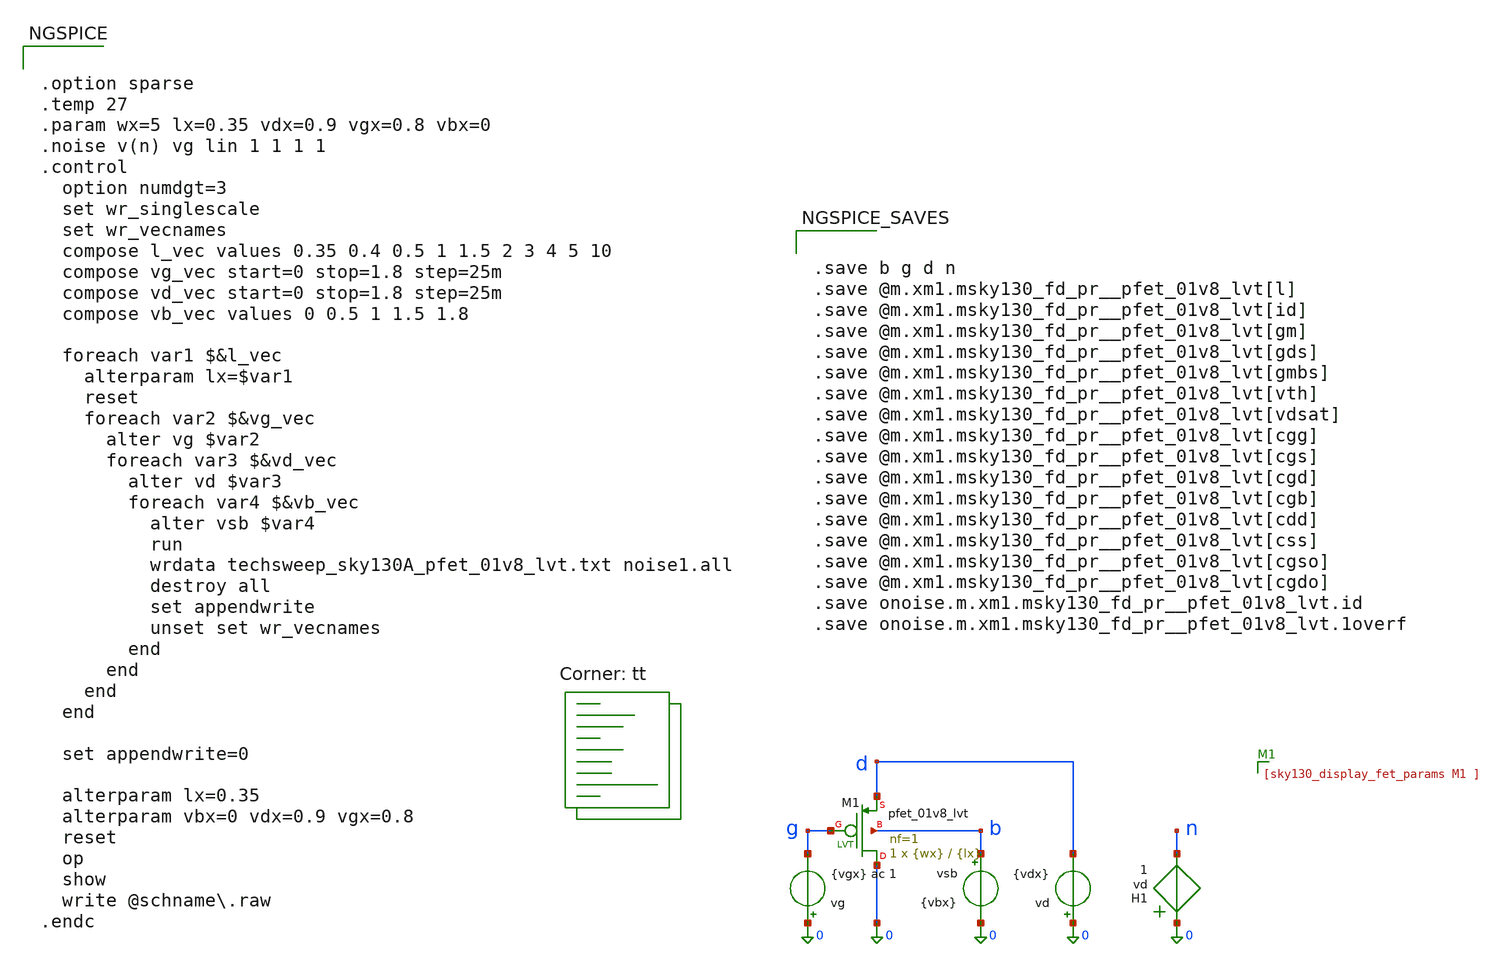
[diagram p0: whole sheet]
** sch_path: sch/gmid/gmid_pmos_lv.sch
**.subckt gmid_pmos_lv
vsb b 0 {vbx}
vd 0 d {vdx}
vg 0 g {vgx} ac 1
H1 0 n vd 1
XM1 0 g d b sky130_fd_pr__pfet_01v8_lvt L={lx} W={wx} nf=1 ad='int((1 + 1)/2) * {wx} / 1 * 0.29' as='int((1 + 2)/2) * {wx} / 1 * 0.29'
+ pd='2*int((1 + 1)/2) * ({wx} / 1 + 0.29)' ps='2*int((1 + 2)/2) * ({wx} / 1 + 0.29)' nrd='0.29 / {wx} '
+ nrs='0.29 / {wx} ' sa=0 sb=0 sd=0 mult=1 m=1
**** begin user architecture code
.lib $::SKYWATER_MODELS/sky130.lib.spice tt


.option sparse
.temp 27
.param wx=5 lx=0.35 vdx=0.9 vgx=0.8 vbx=0
.noise v(n) vg lin 1 1 1 1
.control
  option numdgt=3
  set wr_singlescale
  set wr_vecnames
  compose l_vec values 0.35 0.4 0.5 1 1.5 2 3 4 5 10
  compose vg_vec start=0 stop=1.8 step=25m
  compose vd_vec start=0 stop=1.8 step=25m
  compose vb_vec values 0 0.5 1 1.5 1.8

  foreach var1 $&l_vec
    alterparam lx=$var1
    reset
    foreach var2 $&vg_vec
      alter vg $var2
      foreach var3 $&vd_vec
        alter vd $var3
        foreach var4 $&vb_vec
          alter vsb $var4
          run
          wrdata techsweep_sky130A_pfet_01v8_lvt.txt noise1.all
          destroy all
          set appendwrite
          unset set wr_vecnames
        end
      end
    end
  end

  set appendwrite=0

  alterparam lx=0.35
  alterparam vbx=0 vdx=0.9 vgx=0.8
  reset
  op
  show
  write @schname\.raw
.endc




.save b g d n
.save @m.xm1.msky130_fd_pr__pfet_01v8_lvt[l]
.save @m.xm1.msky130_fd_pr__pfet_01v8_lvt[id]
.save @m.xm1.msky130_fd_pr__pfet_01v8_lvt[gm]
.save @m.xm1.msky130_fd_pr__pfet_01v8_lvt[gds]
.save @m.xm1.msky130_fd_pr__pfet_01v8_lvt[gmbs]
.save @m.xm1.msky130_fd_pr__pfet_01v8_lvt[vth]
.save @m.xm1.msky130_fd_pr__pfet_01v8_lvt[vdsat]
.save @m.xm1.msky130_fd_pr__pfet_01v8_lvt[cgg]
.save @m.xm1.msky130_fd_pr__pfet_01v8_lvt[cgs]
.save @m.xm1.msky130_fd_pr__pfet_01v8_lvt[cgd]
.save @m.xm1.msky130_fd_pr__pfet_01v8_lvt[cgb]
.save @m.xm1.msky130_fd_pr__pfet_01v8_lvt[cdd]
.save @m.xm1.msky130_fd_pr__pfet_01v8_lvt[css]
.save @m.xm1.msky130_fd_pr__pfet_01v8_lvt[cgso]
.save @m.xm1.msky130_fd_pr__pfet_01v8_lvt[cgdo]
.save onoise.m.xm1.msky130_fd_pr__pfet_01v8_lvt.id
.save onoise.m.xm1.msky130_fd_pr__pfet_01v8_lvt.1overf


**** end user architecture code
**.ends
.end
